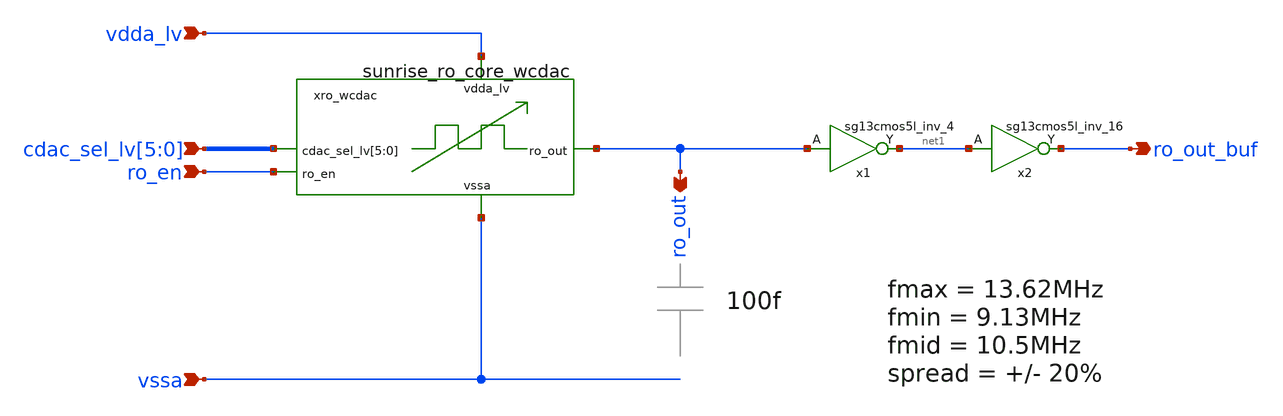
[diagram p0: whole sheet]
** sch_path: Schematics_Layout/sunrise_ro_core_wcdac_buf/sunrise_ro_core_wcdac_buf.sch
**.subckt sunrise_ro_core_wcdac_buf vdda_lv vssa ro_en
*+ cdac_sel_lv[5],cdac_sel_lv[4],cdac_sel_lv[3],cdac_sel_lv[2],cdac_sel_lv[1],cdac_sel_lv[0] ro_out_buf ro_out
*.ipin vdda_lv
*.ipin vssa
*.ipin ro_en
*.ipin cdac_sel_lv[5],cdac_sel_lv[4],cdac_sel_lv[3],cdac_sel_lv[2],cdac_sel_lv[1],cdac_sel_lv[0]
*.opin ro_out_buf
*.opin ro_out
xro_wcdac vdda_lv ro_out ro_en cdac_sel_lv[5] cdac_sel_lv[4] cdac_sel_lv[3] cdac_sel_lv[2]
+ cdac_sel_lv[1] cdac_sel_lv[0] vssa sunrise_ro_core_wcdac
x2 ro_out_buf net1 vdda_lv vssa sg13cmos5l_inv_16
x1 net1 ro_out vdda_lv vssa sg13cmos5l_inv_4
**.ends
.end
